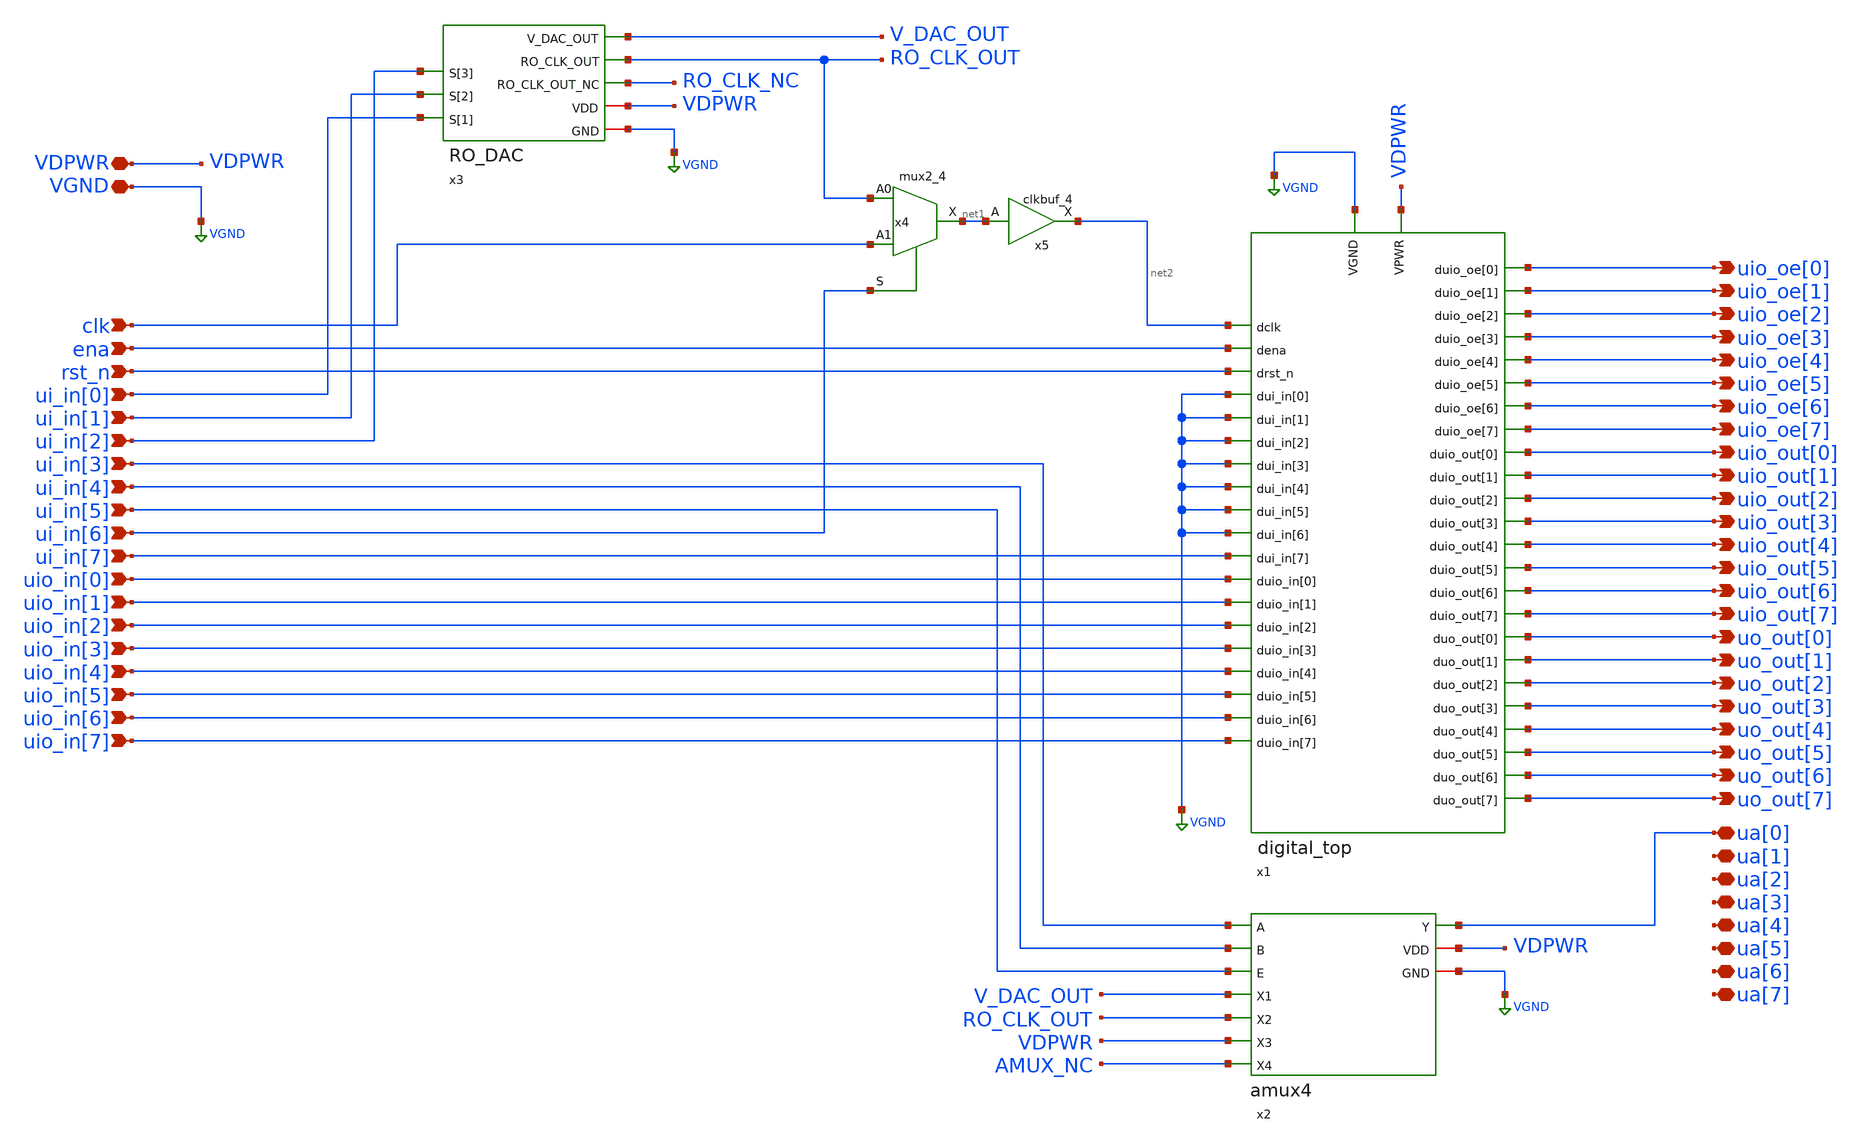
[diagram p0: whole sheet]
** sch_path: src/analog_source_files/tt_um_libormiller_SIMON_V2.sch
**.subckt tt_um_libormiller_SIMON_V2 VDPWR VGND clk ena rst_n ui_in[0] ui_in[1] ui_in[2] ui_in[3]
*+ ui_in[4] ui_in[5] ui_in[6] ui_in[7] uio_in[0] uio_in[1] uio_in[2] uio_in[3] uio_in[4] uio_in[5] uio_in[6]
*+ uio_in[7] uio_oe[0] uio_oe[1] uio_oe[2] uio_oe[3] uio_oe[4] uio_oe[5] uio_oe[6] uio_oe[7] uio_out[0]
*+ uio_out[1] uio_out[2] uio_out[3] uio_out[4] uio_out[5] uio_out[6] uio_out[7] uo_out[0] uo_out[1] uo_out[2]
*+ uo_out[3] uo_out[4] uo_out[5] uo_out[6] uo_out[7] ua[0] ua[1] ua[2] ua[3] ua[4] ua[5] ua[6] ua[7]
*.iopin VDPWR
*.iopin VGND
*.ipin clk
*.ipin ena
*.ipin rst_n
*.ipin ui_in[0]
*.ipin ui_in[1]
*.ipin ui_in[2]
*.ipin ui_in[3]
*.ipin ui_in[4]
*.ipin ui_in[5]
*.ipin ui_in[6]
*.ipin ui_in[7]
*.ipin uio_in[0]
*.ipin uio_in[1]
*.ipin uio_in[2]
*.ipin uio_in[3]
*.ipin uio_in[4]
*.ipin uio_in[5]
*.ipin uio_in[6]
*.ipin uio_in[7]
*.opin uio_oe[0]
*.opin uio_oe[1]
*.opin uio_oe[2]
*.opin uio_oe[3]
*.opin uio_oe[4]
*.opin uio_oe[5]
*.opin uio_oe[6]
*.opin uio_oe[7]
*.opin uio_out[0]
*.opin uio_out[1]
*.opin uio_out[2]
*.opin uio_out[3]
*.opin uio_out[4]
*.opin uio_out[5]
*.opin uio_out[6]
*.opin uio_out[7]
*.opin uo_out[0]
*.opin uo_out[1]
*.opin uo_out[2]
*.opin uo_out[3]
*.opin uo_out[4]
*.opin uo_out[5]
*.opin uo_out[6]
*.opin uo_out[7]
*.iopin ua[0]
*.iopin ua[1]
*.iopin ua[2]
*.iopin ua[3]
*.iopin ua[4]
*.iopin ua[5]
*.iopin ua[6]
*.iopin ua[7]
x1 VGND VDPWR net2 ena rst_n VGND VGND VGND VGND VGND VGND VGND ui_in[7] uio_in[0] uio_in[1]
+ uio_in[2] uio_in[3] uio_in[4] uio_in[5] uio_in[6] uio_in[7] uio_oe[0] uio_oe[1] uio_oe[2] uio_oe[3] uio_oe[4]
+ uio_oe[5] uio_oe[6] uio_oe[7] uio_out[0] uio_out[1] uio_out[2] uio_out[3] uio_out[4] uio_out[5] uio_out[6]
+ uio_out[7] uo_out[0] uo_out[1] uo_out[2] uo_out[3] uo_out[4] uo_out[5] uo_out[6] uo_out[7] digital_top
x2 V_DAC_OUT ui_in[3] ui_in[4] ui_in[5] RO_CLK_OUT ua[0] VDPWR VDPWR VGND AMUX_NC amux4
x3 RO_CLK_OUT ui_in[2] RO_CLK_NC ui_in[1] ui_in[0] VDPWR VGND V_DAC_OUT RO_DAC
x4 RO_CLK_OUT clk ui_in[6] VGND VGND VDPWR VDPWR net1 sky130_fd_sc_hd__mux2_4
x5 net1 VGND VGND VDPWR VDPWR net2 sky130_fd_sc_hd__clkbuf_4
**.ends
.GLOBAL VGND
.end
